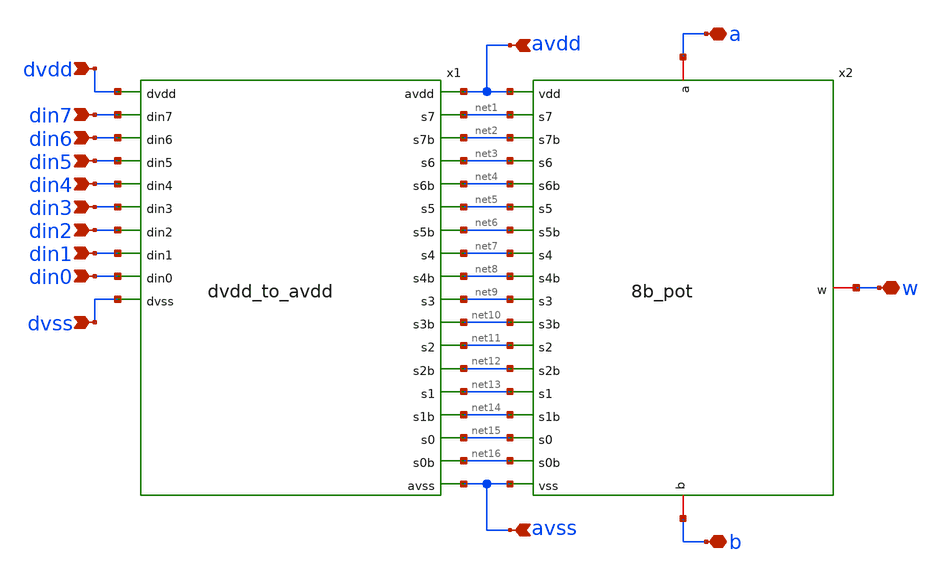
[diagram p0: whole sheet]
** sch_path: xschem/sky130_di_ip__rheostat_8bit.sch
**.subckt sky130_di_ip__rheostat_8bit avdd dvdd dvss avss b w a din0 din1 din2 din3 din4 din5 din6
*+ din7
*.ipin avdd
*.ipin dvdd
*.ipin dvss
*.ipin avss
*.iopin b
*.iopin w
*.iopin a
*.ipin din0
*.ipin din1
*.ipin din2
*.ipin din3
*.ipin din4
*.ipin din5
*.ipin din6
*.ipin din7
x1 avdd dvdd net1 din7 net2 net3 din6 net4 net5 din5 net6 net7 din4 net8 net9 din3 net10 net11 din2
+ net12 net13 din1 net14 net15 din0 net16 dvss avss dvdd_to_avdd
x2 avdd a net1 net2 net3 net4 net5 net6 net7 net8 w net9 net10 net11 net12 net13 net14 net15 net16 b
+ avss 8b_pot
**.ends
.end
